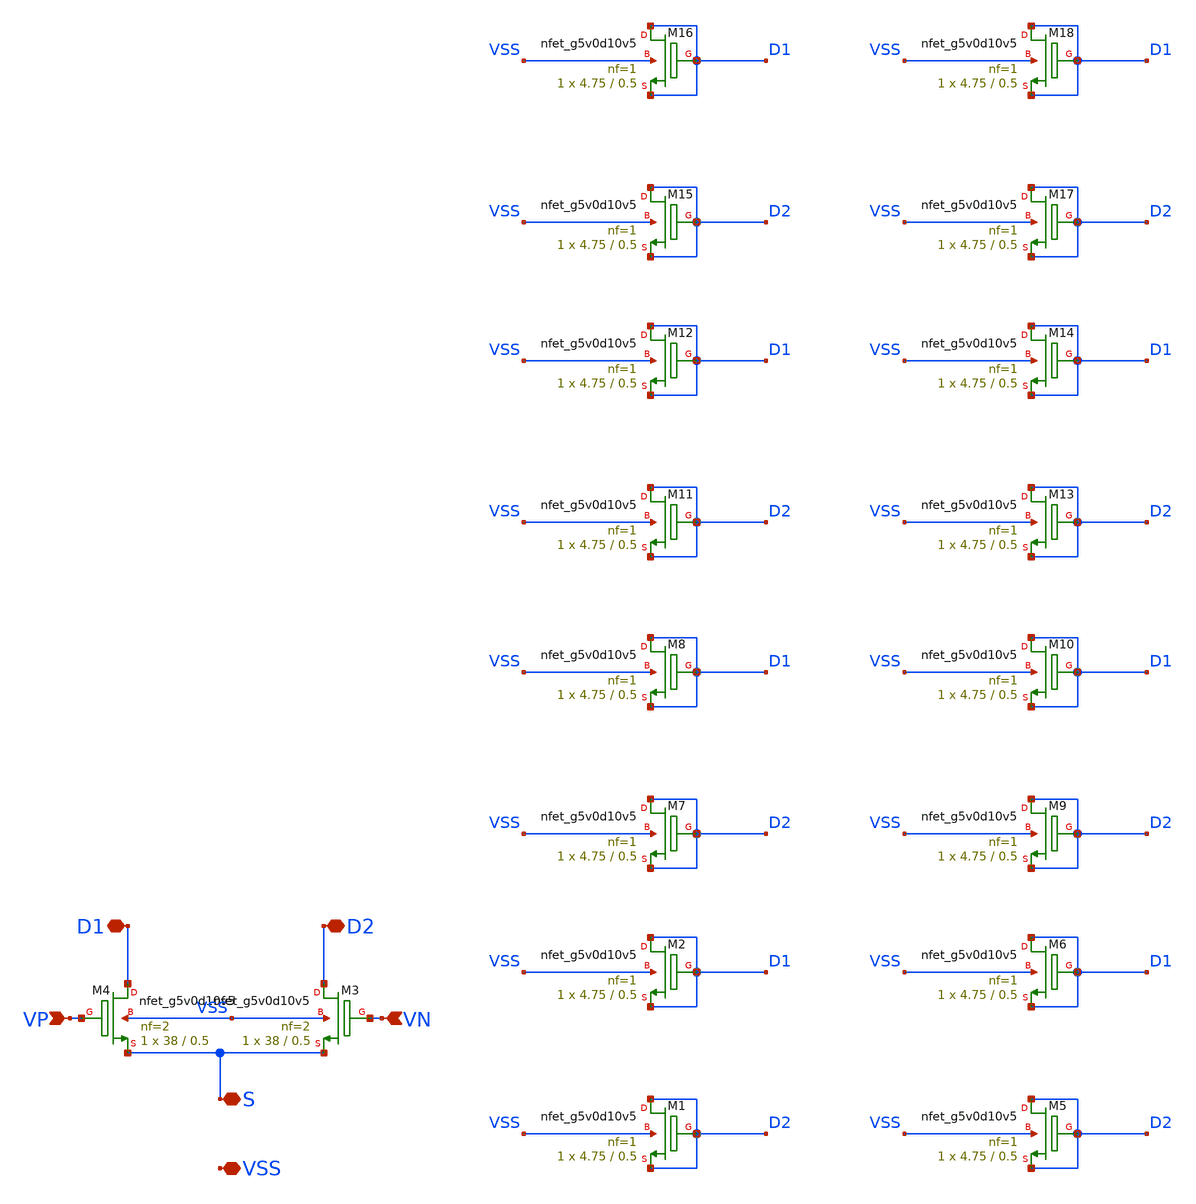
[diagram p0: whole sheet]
** sch_path: xschem/error-amplifier/schematics/sub-blocks/diff-pair.sch
**.subckt diff-pair VP VN S D2 D1 VSS
*.ipin VP
*.ipin VN
*.iopin S
*.iopin D2
*.iopin D1
*.iopin VSS
XM3 D2 VN S VSS sky130_fd_pr__nfet_g5v0d10v5 L=0.5 W=38 nf=2 ad='int((nf+1)/2) * W/nf * 0.29' as='int((nf+2)/2) * W/nf * 0.29'
+ pd='2*int((nf+1)/2) * (W/nf + 0.29)' ps='2*int((nf+2)/2) * (W/nf + 0.29)' nrd='0.29 / W' nrs='0.29 / W'
+ sa=0 sb=0 sd=0 mult=1 m=1
XM4 D1 VP S VSS sky130_fd_pr__nfet_g5v0d10v5 L=0.5 W=38 nf=2 ad='int((nf+1)/2) * W/nf * 0.29' as='int((nf+2)/2) * W/nf * 0.29'
+ pd='2*int((nf+1)/2) * (W/nf + 0.29)' ps='2*int((nf+2)/2) * (W/nf + 0.29)' nrd='0.29 / W' nrs='0.29 / W'
+ sa=0 sb=0 sd=0 mult=1 m=1
XM1 D2 D2 D2 VSS sky130_fd_pr__nfet_g5v0d10v5 L=0.5 W=4.75 nf=1 ad='int((nf+1)/2) * W/nf * 0.29' as='int((nf+2)/2) * W/nf * 0.29'
+ pd='2*int((nf+1)/2) * (W/nf + 0.29)' ps='2*int((nf+2)/2) * (W/nf + 0.29)' nrd='0.29 / W' nrs='0.29 / W'
+ sa=0 sb=0 sd=0 mult=1 m=1
XM2 D1 D1 D1 VSS sky130_fd_pr__nfet_g5v0d10v5 L=0.5 W=4.75 nf=1 ad='int((nf+1)/2) * W/nf * 0.29' as='int((nf+2)/2) * W/nf * 0.29'
+ pd='2*int((nf+1)/2) * (W/nf + 0.29)' ps='2*int((nf+2)/2) * (W/nf + 0.29)' nrd='0.29 / W' nrs='0.29 / W'
+ sa=0 sb=0 sd=0 mult=1 m=1
XM5 D2 D2 D2 VSS sky130_fd_pr__nfet_g5v0d10v5 L=0.5 W=4.75 nf=1 ad='int((nf+1)/2) * W/nf * 0.29' as='int((nf+2)/2) * W/nf * 0.29'
+ pd='2*int((nf+1)/2) * (W/nf + 0.29)' ps='2*int((nf+2)/2) * (W/nf + 0.29)' nrd='0.29 / W' nrs='0.29 / W'
+ sa=0 sb=0 sd=0 mult=1 m=1
XM6 D1 D1 D1 VSS sky130_fd_pr__nfet_g5v0d10v5 L=0.5 W=4.75 nf=1 ad='int((nf+1)/2) * W/nf * 0.29' as='int((nf+2)/2) * W/nf * 0.29'
+ pd='2*int((nf+1)/2) * (W/nf + 0.29)' ps='2*int((nf+2)/2) * (W/nf + 0.29)' nrd='0.29 / W' nrs='0.29 / W'
+ sa=0 sb=0 sd=0 mult=1 m=1
XM7 D2 D2 D2 VSS sky130_fd_pr__nfet_g5v0d10v5 L=0.5 W=4.75 nf=1 ad='int((nf+1)/2) * W/nf * 0.29' as='int((nf+2)/2) * W/nf * 0.29'
+ pd='2*int((nf+1)/2) * (W/nf + 0.29)' ps='2*int((nf+2)/2) * (W/nf + 0.29)' nrd='0.29 / W' nrs='0.29 / W'
+ sa=0 sb=0 sd=0 mult=1 m=1
XM8 D1 D1 D1 VSS sky130_fd_pr__nfet_g5v0d10v5 L=0.5 W=4.75 nf=1 ad='int((nf+1)/2) * W/nf * 0.29' as='int((nf+2)/2) * W/nf * 0.29'
+ pd='2*int((nf+1)/2) * (W/nf + 0.29)' ps='2*int((nf+2)/2) * (W/nf + 0.29)' nrd='0.29 / W' nrs='0.29 / W'
+ sa=0 sb=0 sd=0 mult=1 m=1
XM9 D2 D2 D2 VSS sky130_fd_pr__nfet_g5v0d10v5 L=0.5 W=4.75 nf=1 ad='int((nf+1)/2) * W/nf * 0.29' as='int((nf+2)/2) * W/nf * 0.29'
+ pd='2*int((nf+1)/2) * (W/nf + 0.29)' ps='2*int((nf+2)/2) * (W/nf + 0.29)' nrd='0.29 / W' nrs='0.29 / W'
+ sa=0 sb=0 sd=0 mult=1 m=1
XM10 D1 D1 D1 VSS sky130_fd_pr__nfet_g5v0d10v5 L=0.5 W=4.75 nf=1 ad='int((nf+1)/2) * W/nf * 0.29' as='int((nf+2)/2) * W/nf * 0.29'
+ pd='2*int((nf+1)/2) * (W/nf + 0.29)' ps='2*int((nf+2)/2) * (W/nf + 0.29)' nrd='0.29 / W' nrs='0.29 / W'
+ sa=0 sb=0 sd=0 mult=1 m=1
XM11 D2 D2 D2 VSS sky130_fd_pr__nfet_g5v0d10v5 L=0.5 W=4.75 nf=1 ad='int((nf+1)/2) * W/nf * 0.29' as='int((nf+2)/2) * W/nf * 0.29'
+ pd='2*int((nf+1)/2) * (W/nf + 0.29)' ps='2*int((nf+2)/2) * (W/nf + 0.29)' nrd='0.29 / W' nrs='0.29 / W'
+ sa=0 sb=0 sd=0 mult=1 m=1
XM12 D1 D1 D1 VSS sky130_fd_pr__nfet_g5v0d10v5 L=0.5 W=4.75 nf=1 ad='int((nf+1)/2) * W/nf * 0.29' as='int((nf+2)/2) * W/nf * 0.29'
+ pd='2*int((nf+1)/2) * (W/nf + 0.29)' ps='2*int((nf+2)/2) * (W/nf + 0.29)' nrd='0.29 / W' nrs='0.29 / W'
+ sa=0 sb=0 sd=0 mult=1 m=1
XM13 D2 D2 D2 VSS sky130_fd_pr__nfet_g5v0d10v5 L=0.5 W=4.75 nf=1 ad='int((nf+1)/2) * W/nf * 0.29' as='int((nf+2)/2) * W/nf * 0.29'
+ pd='2*int((nf+1)/2) * (W/nf + 0.29)' ps='2*int((nf+2)/2) * (W/nf + 0.29)' nrd='0.29 / W' nrs='0.29 / W'
+ sa=0 sb=0 sd=0 mult=1 m=1
XM14 D1 D1 D1 VSS sky130_fd_pr__nfet_g5v0d10v5 L=0.5 W=4.75 nf=1 ad='int((nf+1)/2) * W/nf * 0.29' as='int((nf+2)/2) * W/nf * 0.29'
+ pd='2*int((nf+1)/2) * (W/nf + 0.29)' ps='2*int((nf+2)/2) * (W/nf + 0.29)' nrd='0.29 / W' nrs='0.29 / W'
+ sa=0 sb=0 sd=0 mult=1 m=1
XM15 D2 D2 D2 VSS sky130_fd_pr__nfet_g5v0d10v5 L=0.5 W=4.75 nf=1 ad='int((nf+1)/2) * W/nf * 0.29' as='int((nf+2)/2) * W/nf * 0.29'
+ pd='2*int((nf+1)/2) * (W/nf + 0.29)' ps='2*int((nf+2)/2) * (W/nf + 0.29)' nrd='0.29 / W' nrs='0.29 / W'
+ sa=0 sb=0 sd=0 mult=1 m=1
XM16 D1 D1 D1 VSS sky130_fd_pr__nfet_g5v0d10v5 L=0.5 W=4.75 nf=1 ad='int((nf+1)/2) * W/nf * 0.29' as='int((nf+2)/2) * W/nf * 0.29'
+ pd='2*int((nf+1)/2) * (W/nf + 0.29)' ps='2*int((nf+2)/2) * (W/nf + 0.29)' nrd='0.29 / W' nrs='0.29 / W'
+ sa=0 sb=0 sd=0 mult=1 m=1
XM17 D2 D2 D2 VSS sky130_fd_pr__nfet_g5v0d10v5 L=0.5 W=4.75 nf=1 ad='int((nf+1)/2) * W/nf * 0.29' as='int((nf+2)/2) * W/nf * 0.29'
+ pd='2*int((nf+1)/2) * (W/nf + 0.29)' ps='2*int((nf+2)/2) * (W/nf + 0.29)' nrd='0.29 / W' nrs='0.29 / W'
+ sa=0 sb=0 sd=0 mult=1 m=1
XM18 D1 D1 D1 VSS sky130_fd_pr__nfet_g5v0d10v5 L=0.5 W=4.75 nf=1 ad='int((nf+1)/2) * W/nf * 0.29' as='int((nf+2)/2) * W/nf * 0.29'
+ pd='2*int((nf+1)/2) * (W/nf + 0.29)' ps='2*int((nf+2)/2) * (W/nf + 0.29)' nrd='0.29 / W' nrs='0.29 / W'
+ sa=0 sb=0 sd=0 mult=1 m=1
**.ends
.end
